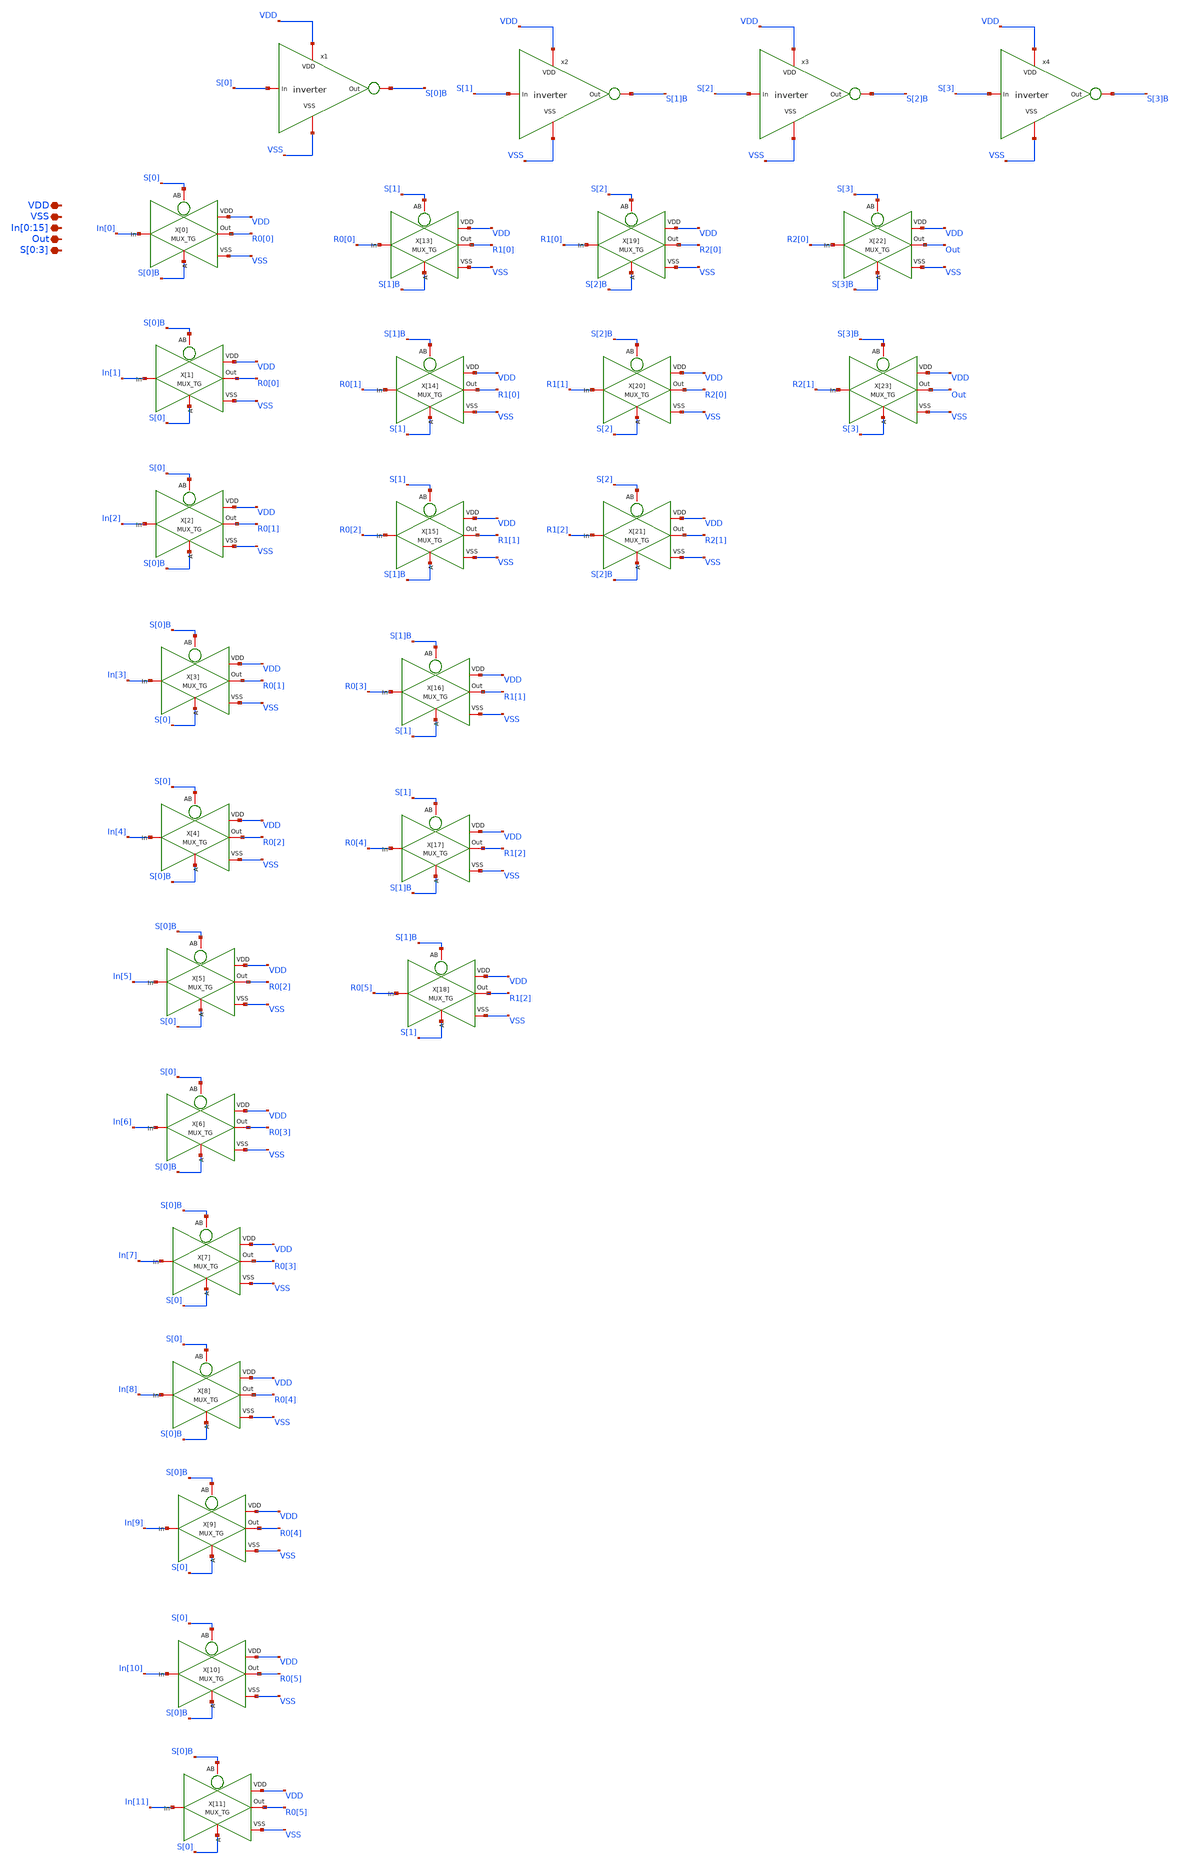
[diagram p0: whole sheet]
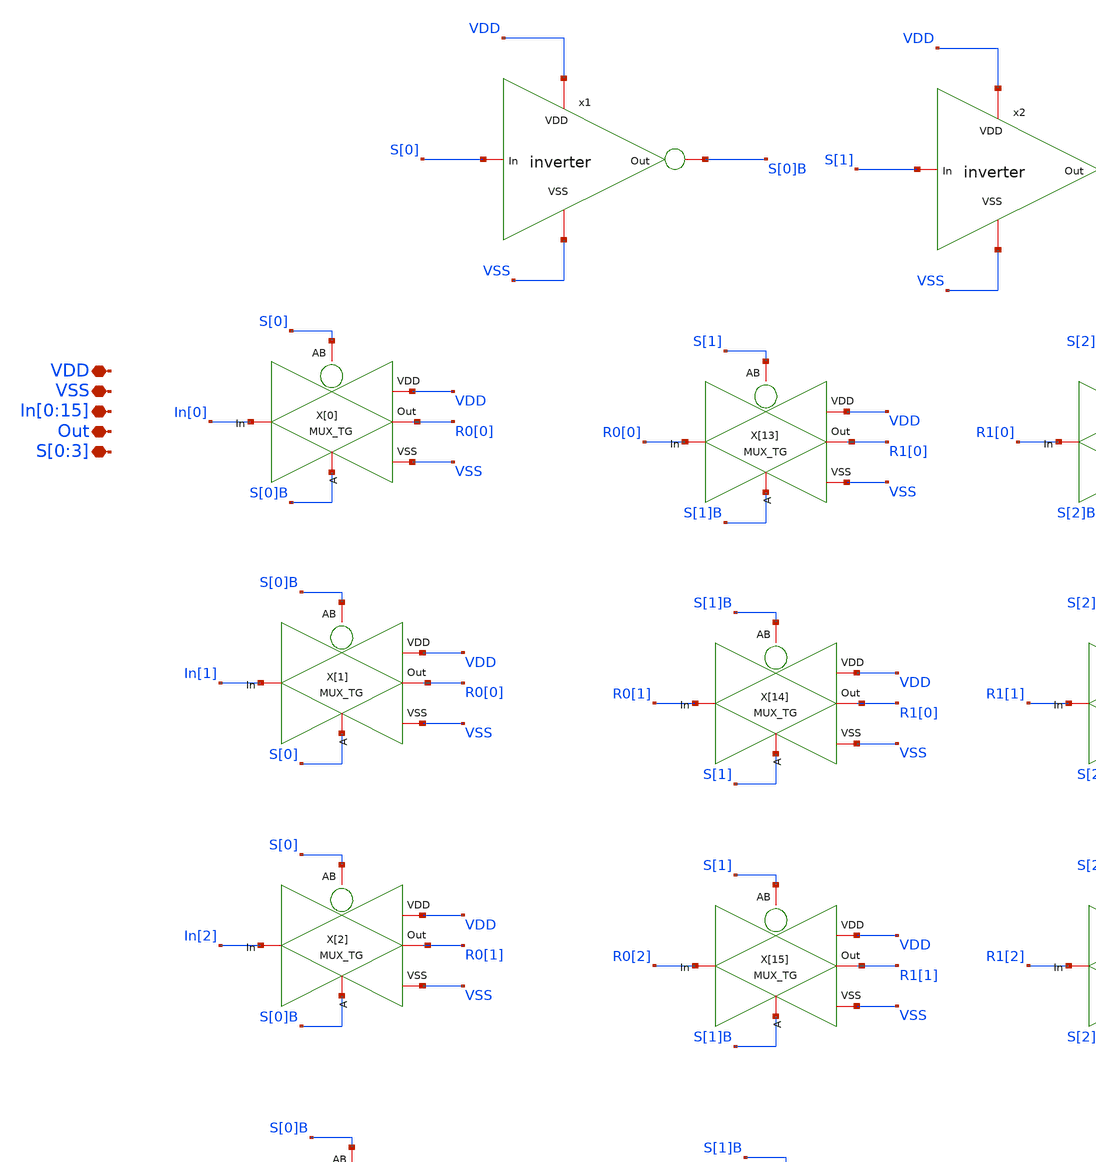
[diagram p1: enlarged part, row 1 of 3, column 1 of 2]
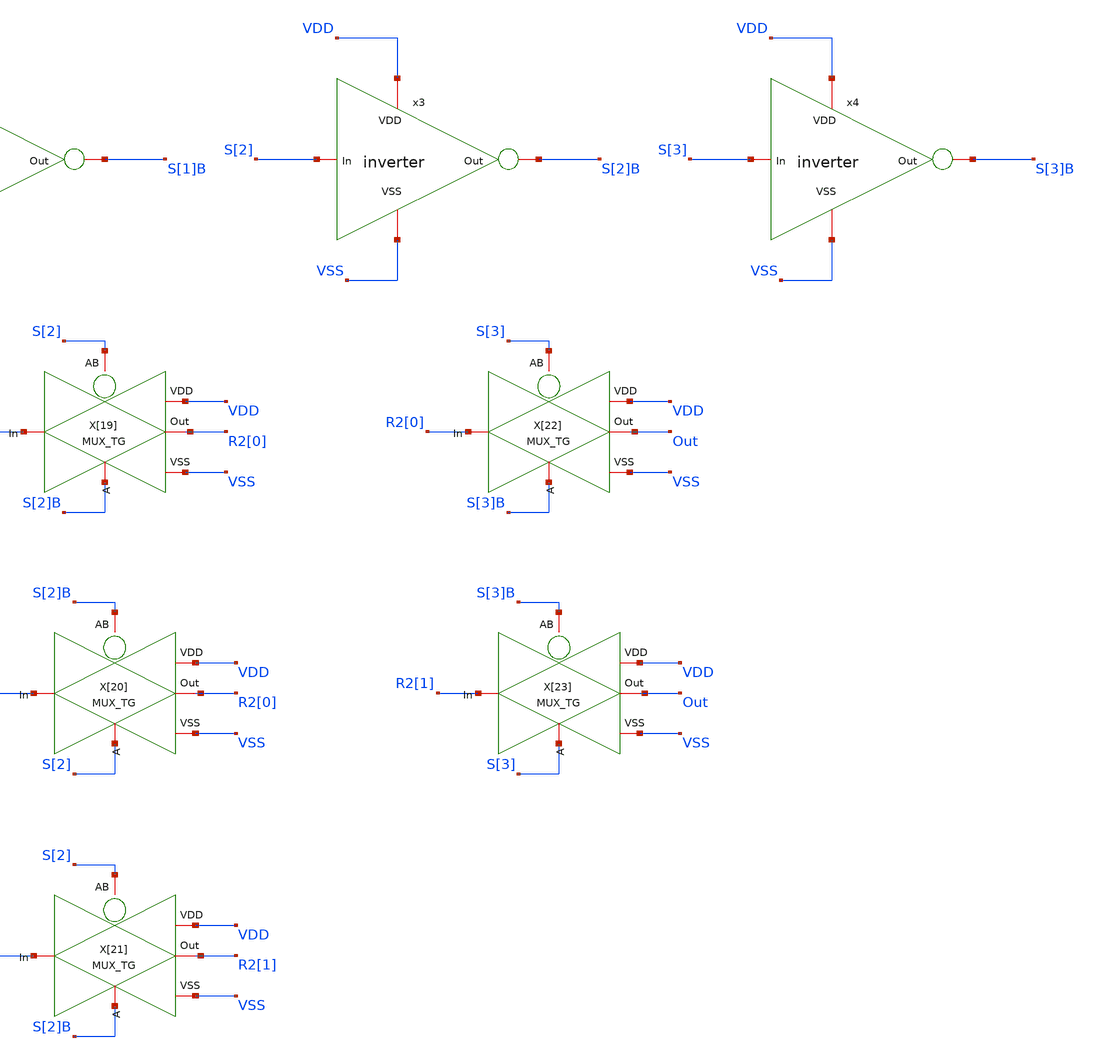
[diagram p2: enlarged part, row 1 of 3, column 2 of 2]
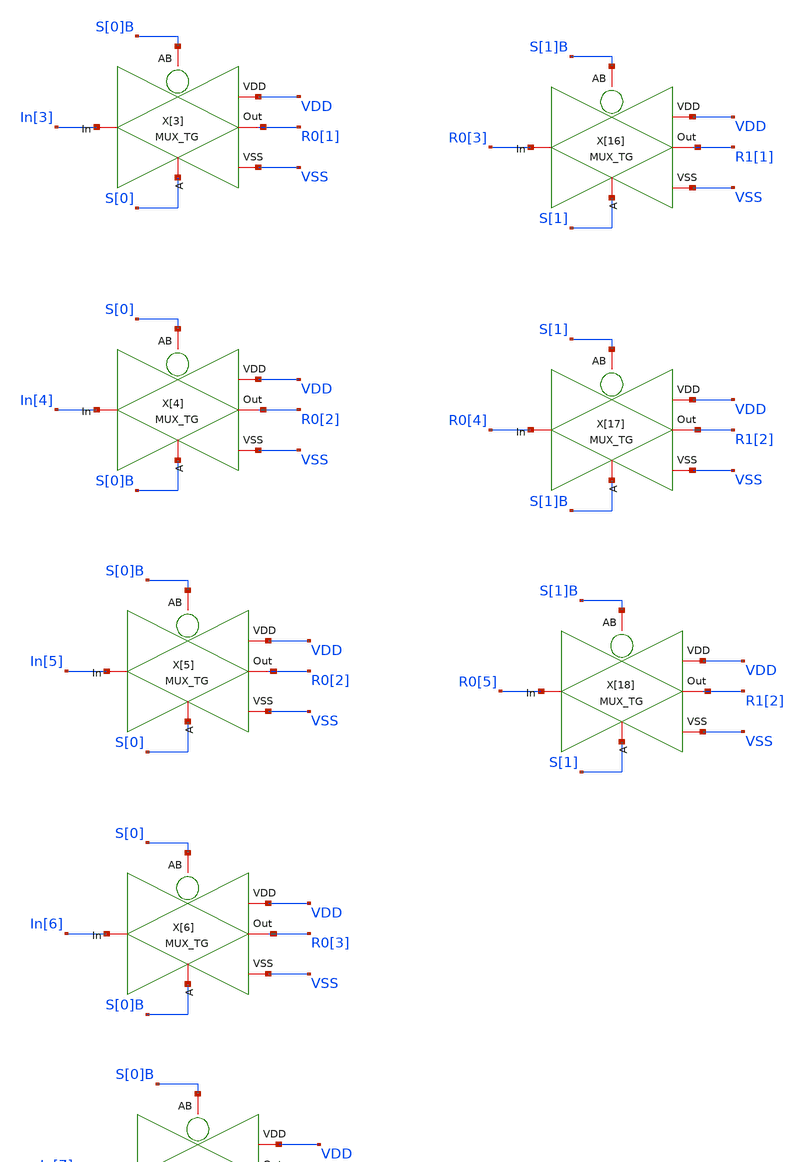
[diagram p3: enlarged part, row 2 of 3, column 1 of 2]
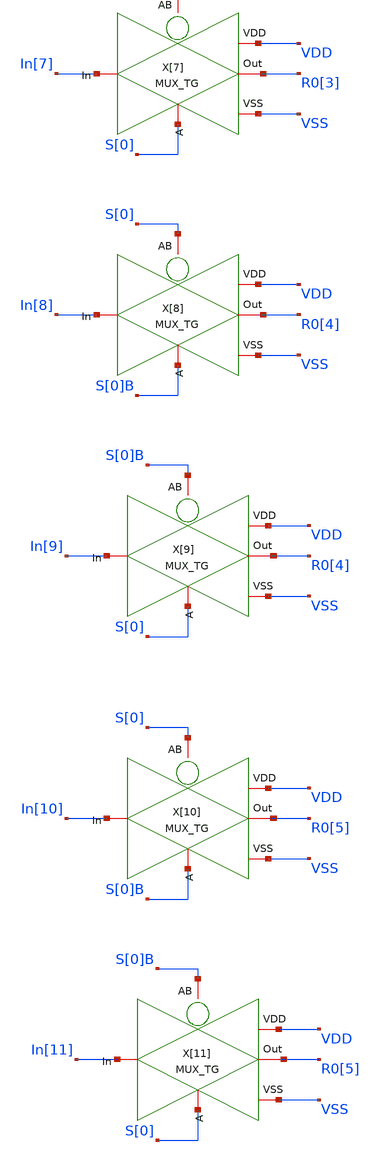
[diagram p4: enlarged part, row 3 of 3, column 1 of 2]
** sch_path: MUX/MUX.sch
**.subckt MUX VDD VSS
*+ In[0],In[1],In[2],In[3],In[4],In[5],In[6],In[7],In[8],In[9],In[10],In[11],In[12],In[13],In[14],In[15] Out S[0],S[1],S[2],S[3]
*.iopin VDD
*.iopin VSS
*.iopin
*+ In[0],In[1],In[2],In[3],In[4],In[5],In[6],In[7],In[8],In[9],In[10],In[11],In[12],In[13],In[14],In[15]
*.iopin Out
*.iopin S[0],S[1],S[2],S[3]
X[0] S[0] VDD R0[0] In[0] VSS S[0]B MUX_TG
x1 VDD S[0]B S[0] VSS inverter
X[13] S[1] VDD R1[0] R0[0] VSS S[1]B MUX_TG
x2 VDD S[1]B S[1] VSS inverter
X[19] S[2] VDD R2[0] R1[0] VSS S[2]B MUX_TG
x3 VDD S[2]B S[2] VSS inverter
x4 VDD S[3]B S[3] VSS inverter
X[22] S[3] VDD Out R2[0] VSS S[3]B MUX_TG
X[1] S[0]B VDD R0[0] In[1] VSS S[0] MUX_TG
X[14] S[1]B VDD R1[0] R0[1] VSS S[1] MUX_TG
X[20] S[2]B VDD R2[0] R1[1] VSS S[2] MUX_TG
X[23] S[3]B VDD Out R2[1] VSS S[3] MUX_TG
X[2] S[0] VDD R0[1] In[2] VSS S[0]B MUX_TG
X[15] S[1] VDD R1[1] R0[2] VSS S[1]B MUX_TG
X[21] S[2] VDD R2[1] R1[2] VSS S[2]B MUX_TG
X[3] S[0]B VDD R0[1] In[3] VSS S[0] MUX_TG
X[16] S[1]B VDD R1[1] R0[3] VSS S[1] MUX_TG
X[4] S[0] VDD R0[2] In[4] VSS S[0]B MUX_TG
X[17] S[1] VDD R1[2] R0[4] VSS S[1]B MUX_TG
X[5] S[0]B VDD R0[2] In[5] VSS S[0] MUX_TG
X[18] S[1]B VDD R1[2] R0[5] VSS S[1] MUX_TG
X[6] S[0] VDD R0[3] In[6] VSS S[0]B MUX_TG
X[7] S[0]B VDD R0[3] In[7] VSS S[0] MUX_TG
X[8] S[0] VDD R0[4] In[8] VSS S[0]B MUX_TG
X[9] S[0]B VDD R0[4] In[9] VSS S[0] MUX_TG
X[10] S[0] VDD R0[5] In[10] VSS S[0]B MUX_TG
X[11] S[0]B VDD R0[5] In[11] VSS S[0] MUX_TG
**.ends

* expanding   symbol:  MUX_TG.sym # of pins=6
** sym_path: MUX/MUX_TG.sym
** sch_path: MUX/MUX_TG.sch
.subckt MUX_TG AB VDD Out In VSS A
*.iopin In
*.iopin Out
*.iopin VDD
*.iopin VSS
*.iopin AB
*.iopin A
XM1 In A Out VSS sky130_fd_pr__nfet_01v8 L=0.15 W=2.1 nf=1 ad='int((nf+1)/2) * W/nf * 0.29' as='int((nf+2)/2) * W/nf * 0.29'
+ pd='2*int((nf+1)/2) * (W/nf + 0.29)' ps='2*int((nf+2)/2) * (W/nf + 0.29)' nrd='0.29 / W' nrs='0.29 / W'
+ sa=0 sb=0 sd=0 mult=2 m=2
XM2 In AB Out VDD sky130_fd_pr__pfet_01v8 L=0.15 W=4.75 nf=1 ad='int((nf+1)/2) * W/nf * 0.29' as='int((nf+2)/2) * W/nf * 0.29'
+ pd='2*int((nf+1)/2) * (W/nf + 0.29)' ps='2*int((nf+2)/2) * (W/nf + 0.29)' nrd='0.29 / W' nrs='0.29 / W'
+ sa=0 sb=0 sd=0 mult=4 m=4
.ends


* expanding   symbol:  inverter.sym # of pins=4
** sym_path: MUX/inverter.sym
** sch_path: MUX/inverter.sch
.subckt inverter VDD Out In VSS
*.iopin VDD
*.iopin Out
*.iopin VSS
*.iopin In
XM3 Out In VSS VSS sky130_fd_pr__nfet_01v8 L=0.15 W=2.1 nf=1 ad='int((nf+1)/2) * W/nf * 0.29' as='int((nf+2)/2) * W/nf * 0.29'
+ pd='2*int((nf+1)/2) * (W/nf + 0.29)' ps='2*int((nf+2)/2) * (W/nf + 0.29)' nrd='0.29 / W' nrs='0.29 / W'
+ sa=0 sb=0 sd=0 mult=2 m=2
XM1 Out In VDD VDD sky130_fd_pr__pfet_01v8 L=0.15 W=4.75 nf=1 ad='int((nf+1)/2) * W/nf * 0.29' as='int((nf+2)/2) * W/nf * 0.29'
+ pd='2*int((nf+1)/2) * (W/nf + 0.29)' ps='2*int((nf+2)/2) * (W/nf + 0.29)' nrd='0.29 / W' nrs='0.29 / W'
+ sa=0 sb=0 sd=0 mult=4 m=4
.ends

.end
